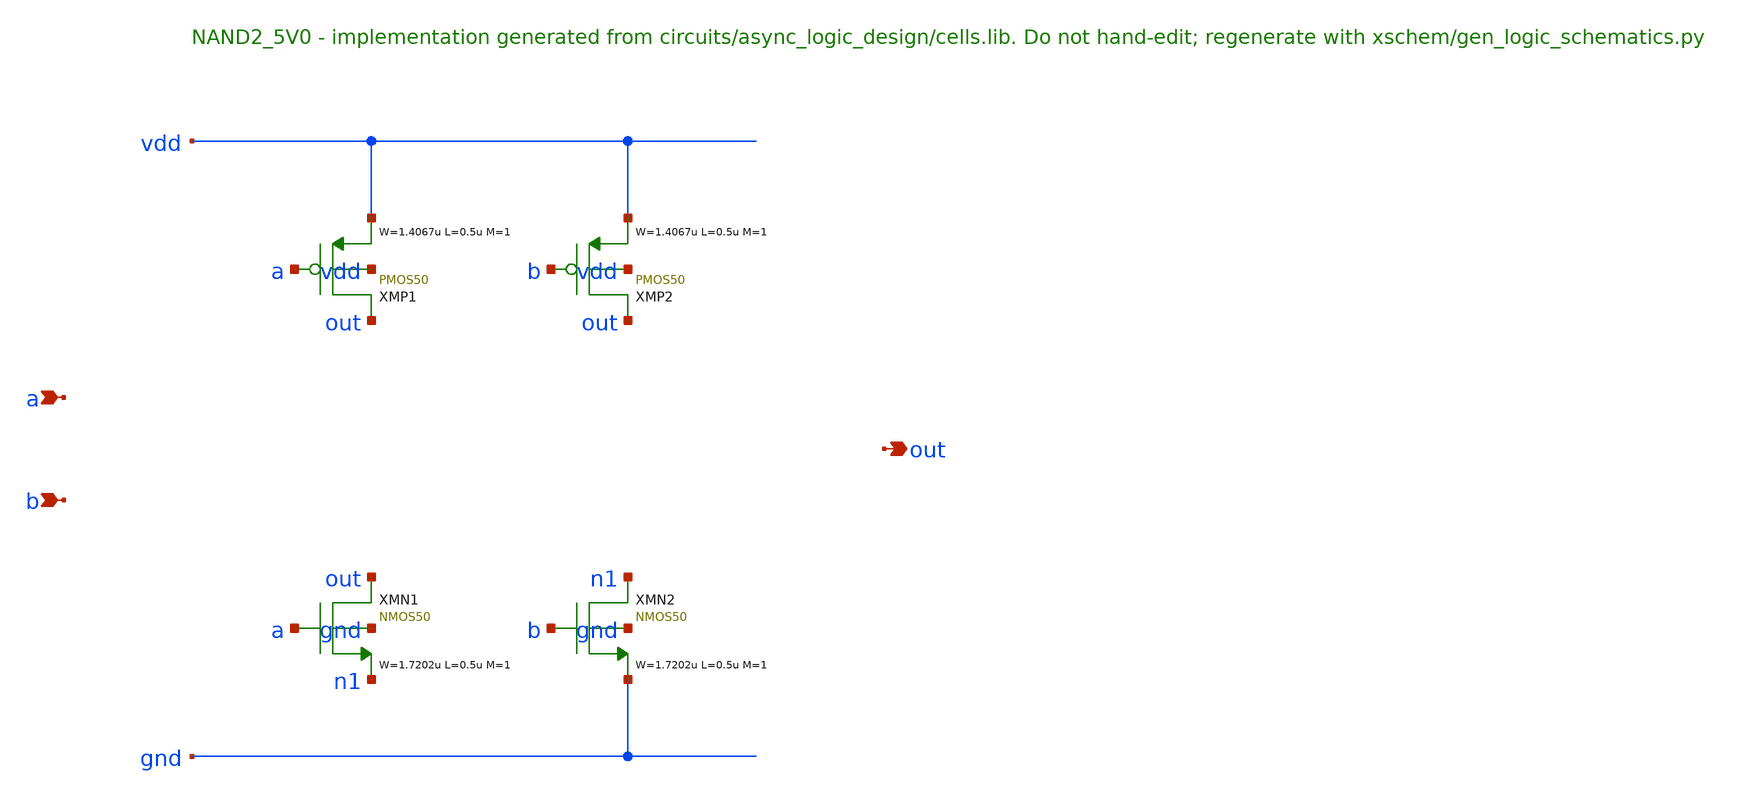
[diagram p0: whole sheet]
** sch_path: xschem/logic/NAND2_5V0.sch
**.subckt NAND2_5V0 a b out
*.ipin a
*.ipin b
*.opin out
XMP1 out a vdd vdd PMOS50 W=1.4067u L=0.5u M=1 MM_SIGMA=0
XMP2 out b vdd vdd PMOS50 W=1.4067u L=0.5u M=1 MM_SIGMA=0
XMN1 out a n1 gnd NMOS50 W=1.7202u L=0.5u M=1 MM_SIGMA=0
XMN2 n1 b gnd gnd NMOS50 W=1.7202u L=0.5u M=1 MM_SIGMA=0
**.ends
.end
